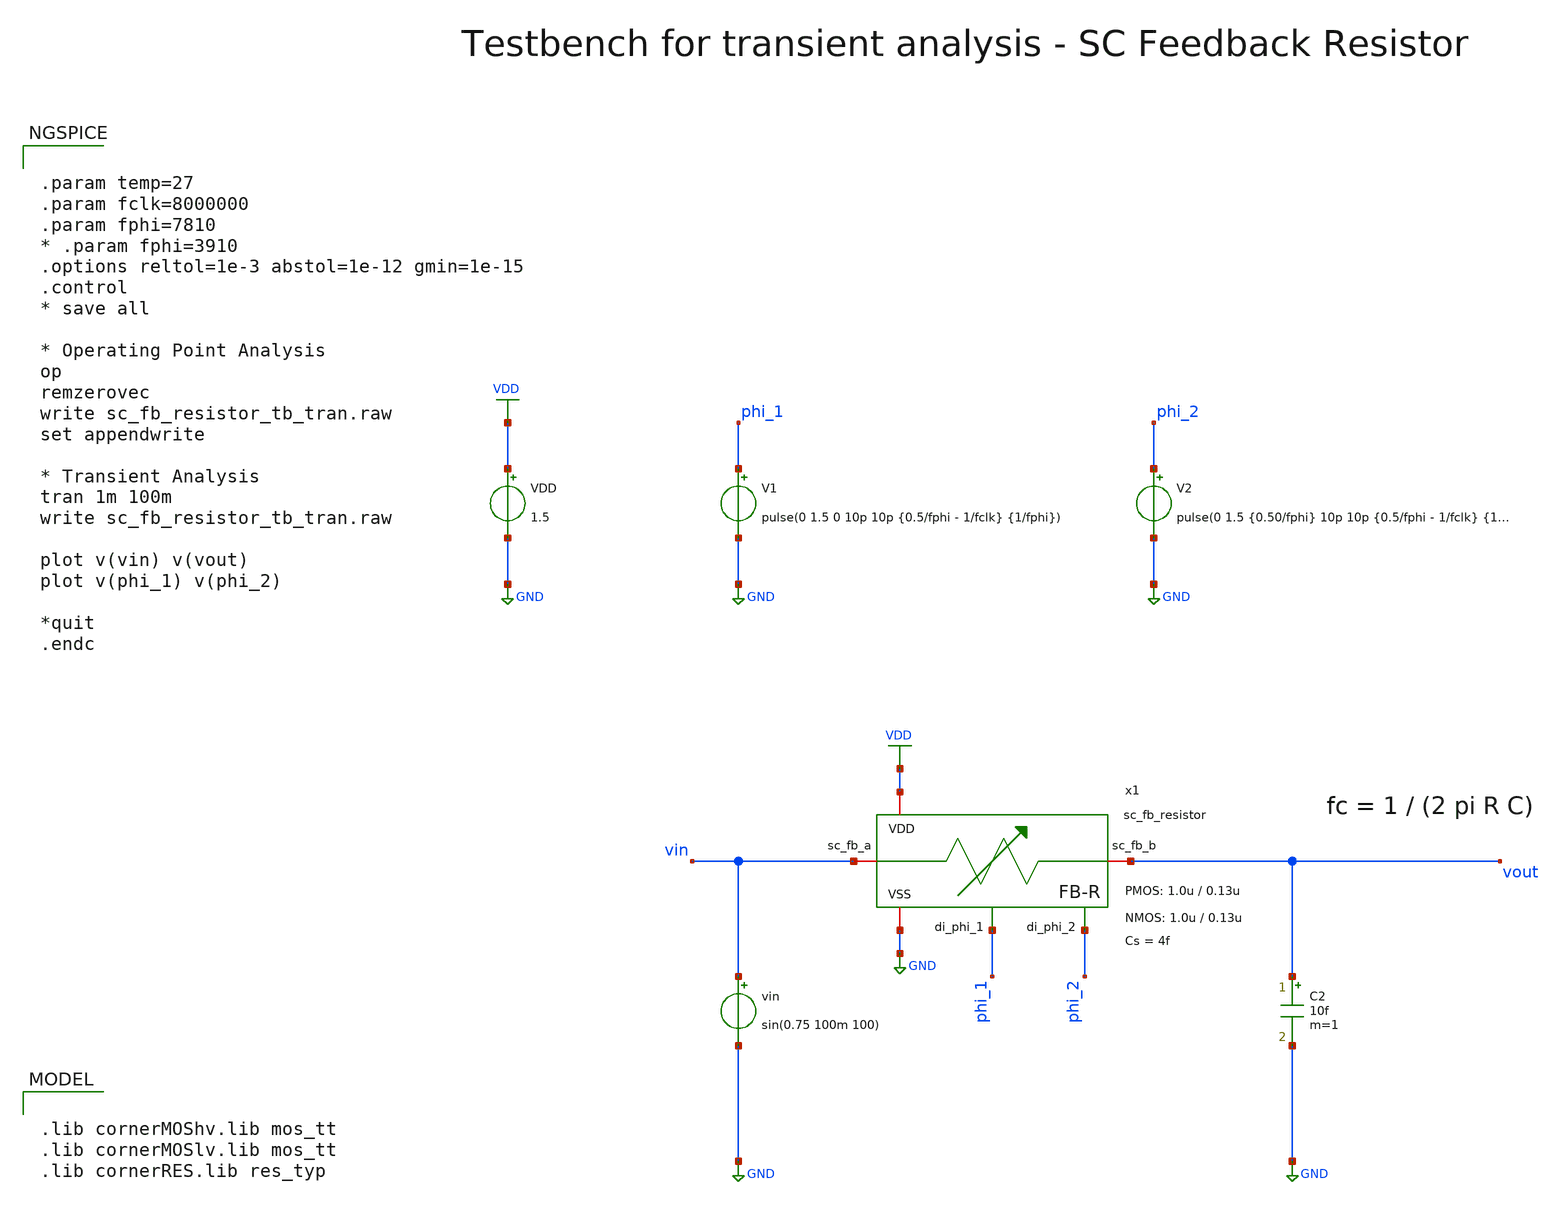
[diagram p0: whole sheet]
** sch_path: SG13G2_ATBS-ADC-main/xschem/bio_amplifier/sc_fb_resistor/testbenches/sc_fb_resistor_tb_tran.sch
**.subckt sc_fb_resistor_tb_tran
vin vin GND sin(0.75 100m 100)
VDD VDD GND 1.5
C2 vout GND 10f m=1
V1 phi_1 GND pulse(0 1.5 0 10p 10p {0.5/fphi - 1/fclk} {1/fphi})
V2 phi_2 GND pulse(0 1.5 {0.50/fphi} 10p 10p {0.5/fphi - 1/fclk} {1/fphi})
x1 vin vout phi_2 phi_1 VDD GND sc_fb_resistor W_P_FB=1.0u L_P_FB=0.13u W_N_FB=1.0u L_N_FB=0.13u
+ Cs=4f
**** begin user architecture code

.lib cornerMOShv.lib mos_tt
.lib cornerMOSlv.lib mos_tt
.lib cornerRES.lib res_typ



.param temp=27
.param fclk=8000000
.param fphi=7810
* .param fphi=3910
.options reltol=1e-3 abstol=1e-12 gmin=1e-15
.control
* save all

* Operating Point Analysis
op
remzerovec
write sc_fb_resistor_tb_tran.raw
set appendwrite

* Transient Analysis
tran 1m 100m
write sc_fb_resistor_tb_tran.raw

plot v(vin) v(vout)
plot v(phi_1) v(phi_2)

*quit
.endc

**** end user architecture code
**.ends

* expanding   symbol:  bio_amplifier/sc_fb_resistor/sc_fb_resistor.sym # of pins=6
** sym_path: SG13G2_ATBS-ADC-main/xschem/bio_amplifier/sc_fb_resistor/sc_fb_resistor.sym
** sch_path: SG13G2_ATBS-ADC-main/xschem/bio_amplifier/sc_fb_resistor/sc_fb_resistor.sch
.subckt sc_fb_resistor sc_fb_a sc_fb_b di_phi_2 di_phi_1 VDD VSS  W_P_FB=1.0u L_P_FB=0.13u
+ W_N_FB=1.0u L_N_FB=0.13u Cs=4f
*.iopin VSS
*.iopin VDD
*.iopin sc_fb_a
*.iopin sc_fb_b
*.ipin di_phi_1
*.ipin di_phi_2
x1 VDD di_phi_1 VSS net1 sc_fb_a di_phi_1_n transmission_gate_lv_wo_dummy W_P=W_P_FB L_P=L_P_FB
+ W_N=W_N_FB L_N=L_N_FB
x2 VDD di_phi_2 VSS net2 net1 di_phi_2_n transmission_gate_lv_wo_dummy W_P=W_P_FB L_P=L_P_FB
+ W_N=W_N_FB L_N=L_N_FB
x3 VDD di_phi_1 VSS net3 net2 di_phi_1_n transmission_gate_lv_wo_dummy W_P=W_P_FB L_P=L_P_FB
+ W_N=W_N_FB L_N=L_N_FB
x4 VDD di_phi_2 VSS net4 net3 di_phi_2_n transmission_gate_lv_wo_dummy W_P=W_P_FB L_P=L_P_FB
+ W_N=W_N_FB L_N=L_N_FB
x5 VDD di_phi_1 VSS net5 net4 di_phi_1_n transmission_gate_lv_wo_dummy W_P=W_P_FB L_P=L_P_FB
+ W_N=W_N_FB L_N=L_N_FB
x6 VDD di_phi_2 VSS sc_fb_b net5 di_phi_2_n transmission_gate_lv_wo_dummy W_P=W_P_FB L_P=L_P_FB
+ W_N=W_N_FB L_N=L_N_FB
C1 net1 VSS Cs m=1
C2 net2 VSS Cs m=1
C3 net3 VSS Cs m=1
C4 net4 VSS Cs m=1
C5 net5 VSS Cs m=1
x7 VDD di_phi_1 di_phi_1_n VSS inverter_lv W_P=W_P_FB L_P=L_P_FB W_N=W_N_FB L_N=L_N_FB
x8 VDD di_phi_2 di_phi_2_n VSS inverter_lv W_P=W_P_FB L_P=L_P_FB W_N=W_N_FB L_N=L_N_FB
.ends


* expanding   symbol:  transmission_gate/transmission_gate_lv_wo_dummy.sym # of pins=6
** sym_path: SG13G2_ATBS-ADC-main/xschem/transmission_gate/transmission_gate_lv_wo_dummy.sym
** sch_path: SG13G2_ATBS-ADC-main/xschem/transmission_gate/transmission_gate_lv_wo_dummy.sch
.subckt transmission_gate_lv_wo_dummy VDD di_tg_ctrl VSS v_b v_a di_tg_ctrl_n  W_P=1.0u L_P=0.13u
+ W_N=1.0u L_N=0.13u
*.iopin v_a
*.iopin v_b
*.iopin VDD
*.iopin VSS
*.ipin di_tg_ctrl
*.ipin di_tg_ctrl_n
XM1 v_a di_tg_ctrl v_b VSS sg13_lv_nmos w=W_N l=L_N ng=1 m=1 mm_ok=1
XM2 v_a di_tg_ctrl_n v_b VDD sg13_lv_pmos w=W_P l=L_P ng=1 m=1 mm_ok=1
.ends


* expanding   symbol:  inverter/inverter_lv.sym # of pins=4
** sym_path: SG13G2_ATBS-ADC-main/xschem/inverter/inverter_lv.sym
** sch_path: SG13G2_ATBS-ADC-main/xschem/inverter/inverter_lv.sch
.subckt inverter_lv VDD vin vout VSS  W_P=3.0u L_P=0.13u W_N=1.0u L_N=0.13u
*.ipin vin
*.iopin VDD
*.iopin VSS
*.opin vout
XM1 vout vin VDD VDD sg13_lv_pmos w=W_P l=L_P ng=1 m=1 mm_ok=1
XM2 vout vin VSS VSS sg13_lv_nmos w=W_N l=L_N ng=1 m=1 mm_ok=1
.ends

.GLOBAL GND
.GLOBAL VDD
.end
